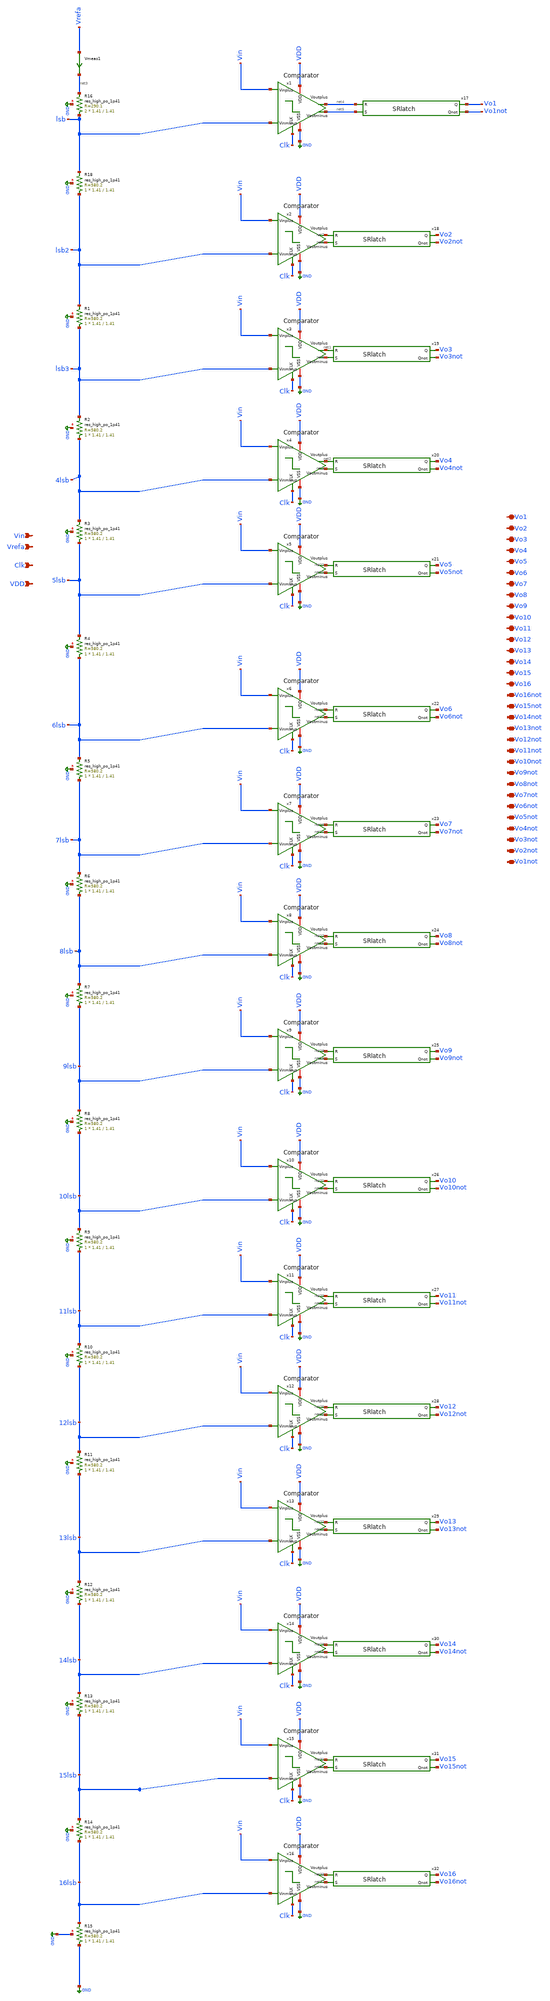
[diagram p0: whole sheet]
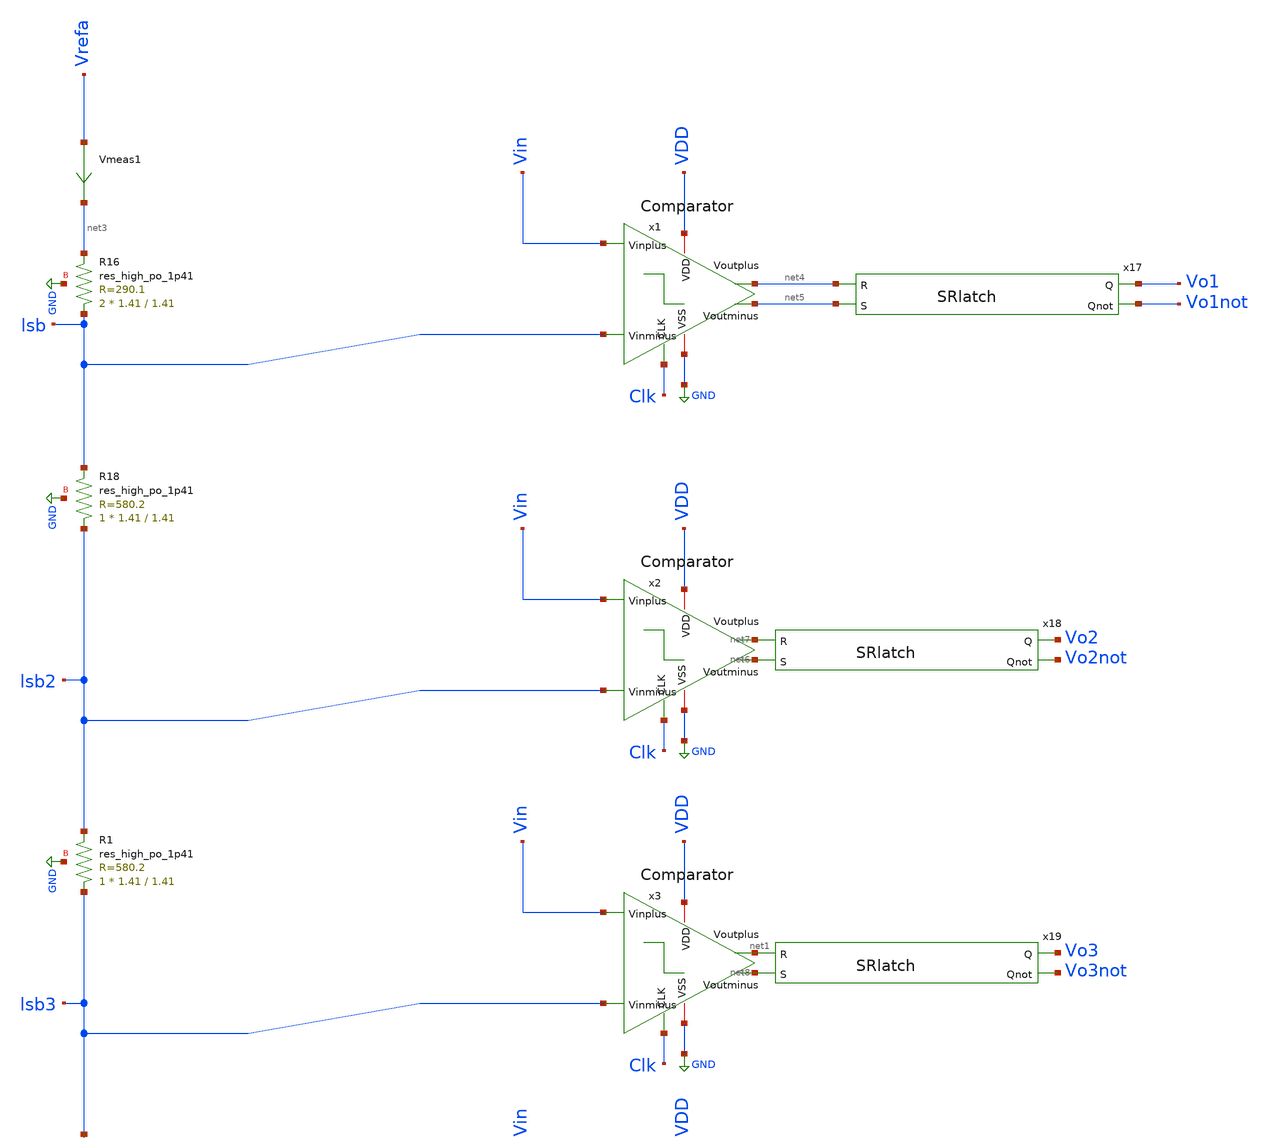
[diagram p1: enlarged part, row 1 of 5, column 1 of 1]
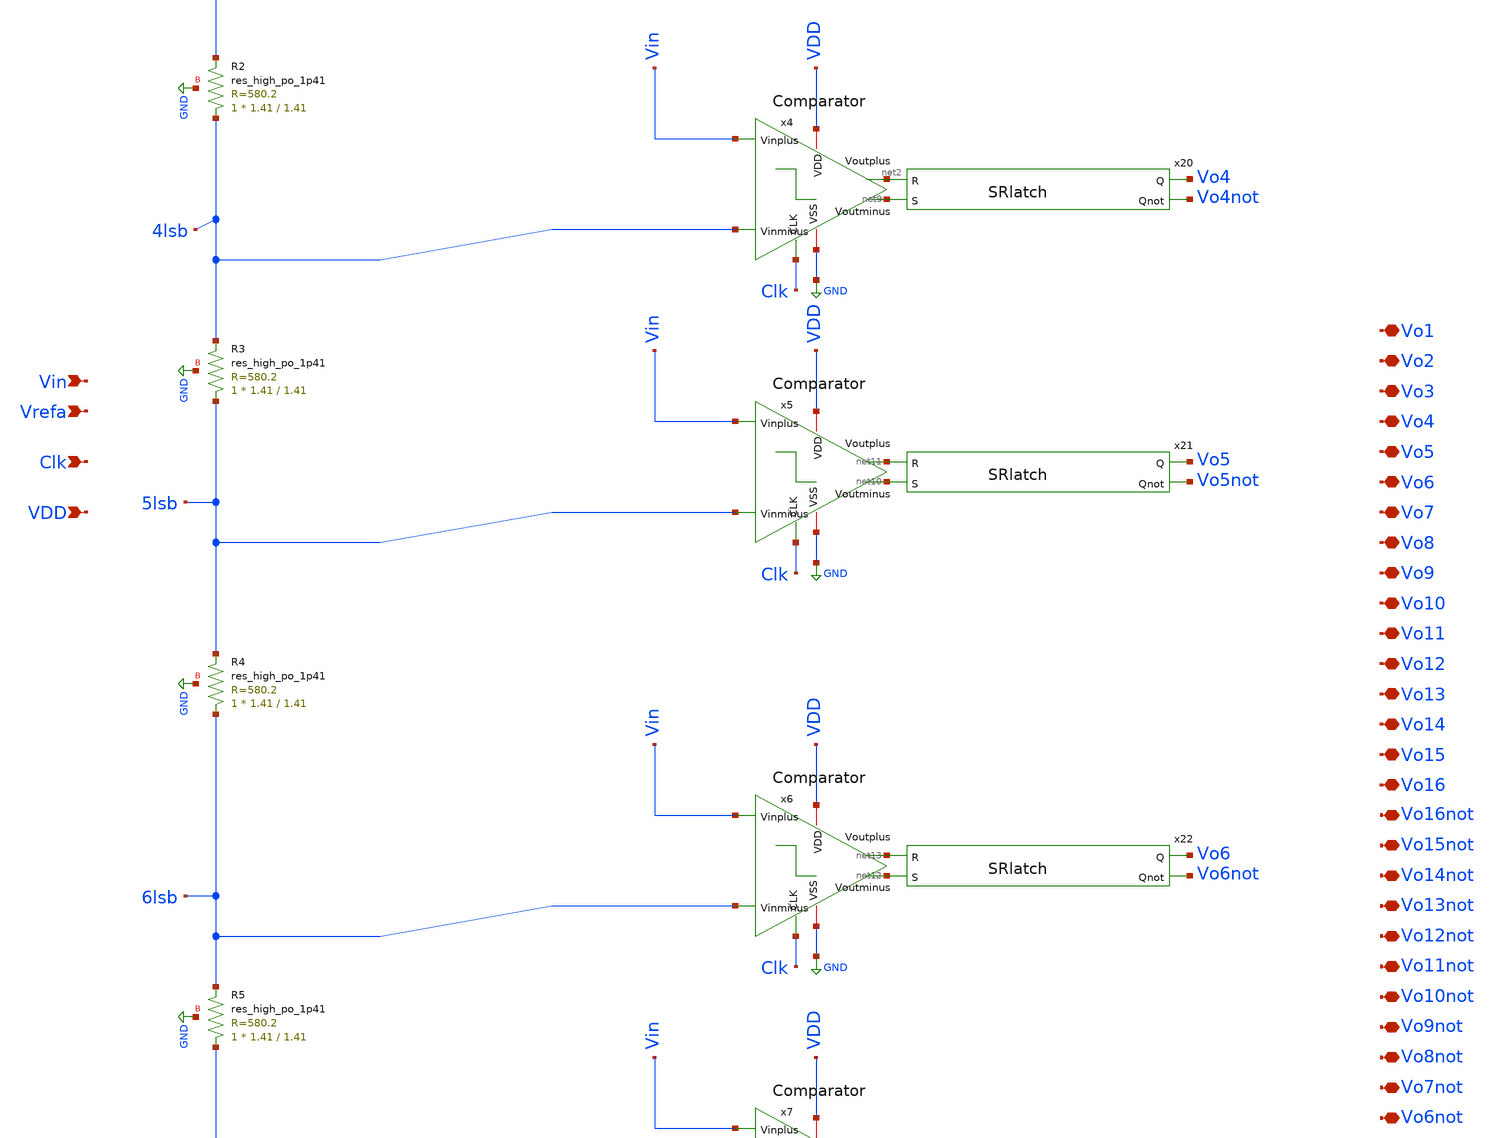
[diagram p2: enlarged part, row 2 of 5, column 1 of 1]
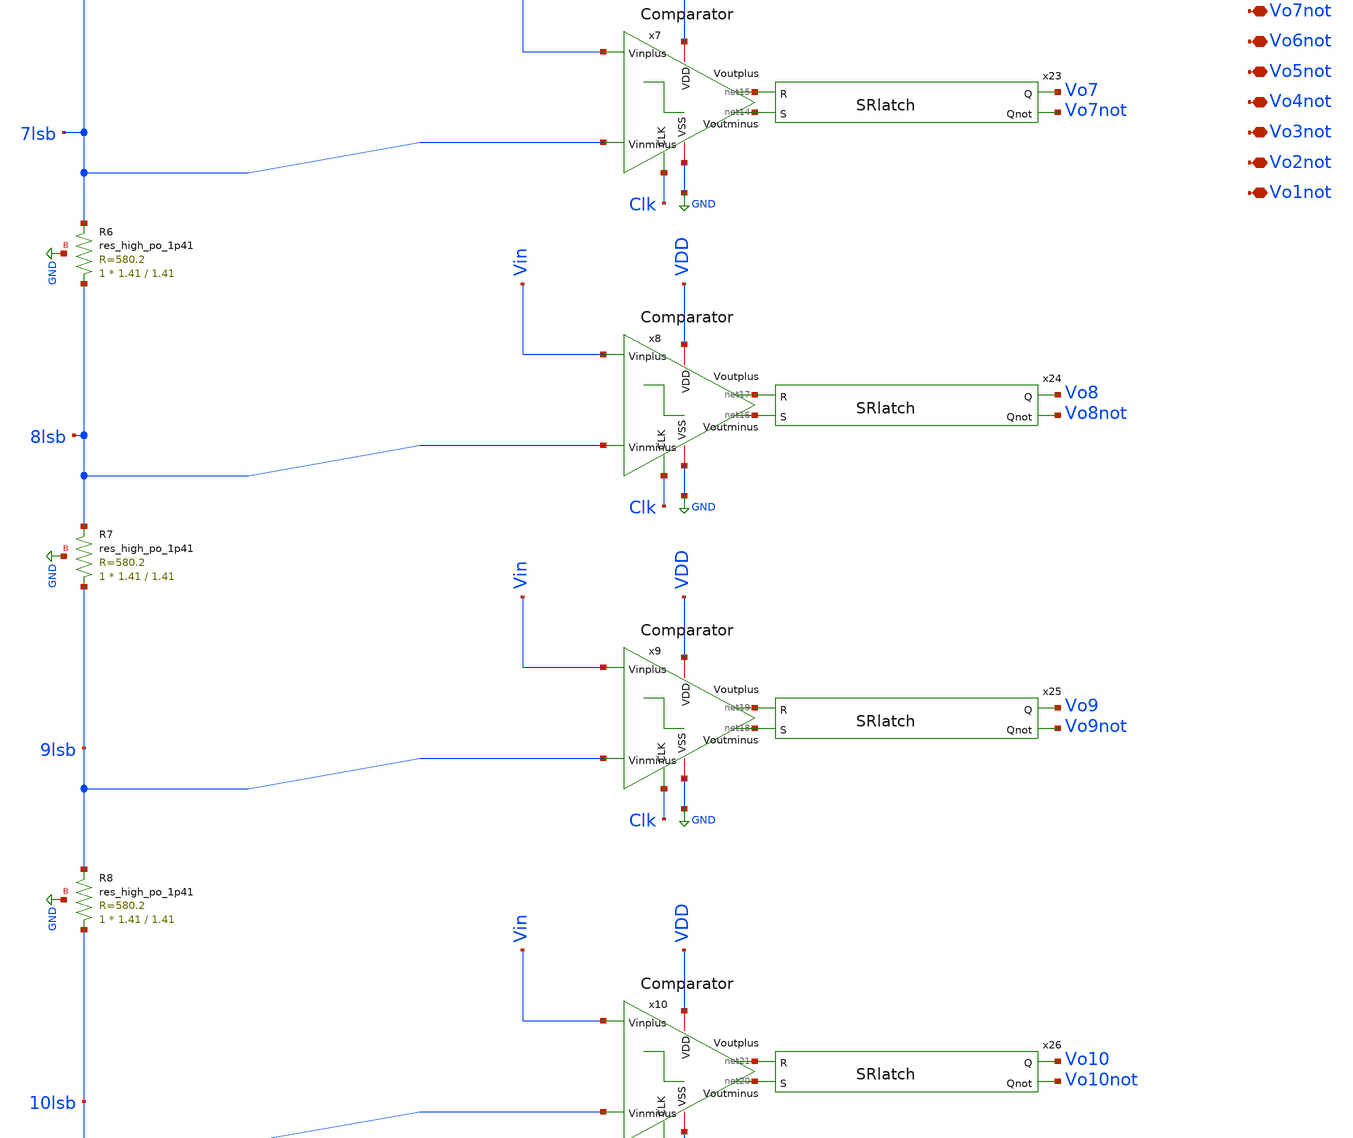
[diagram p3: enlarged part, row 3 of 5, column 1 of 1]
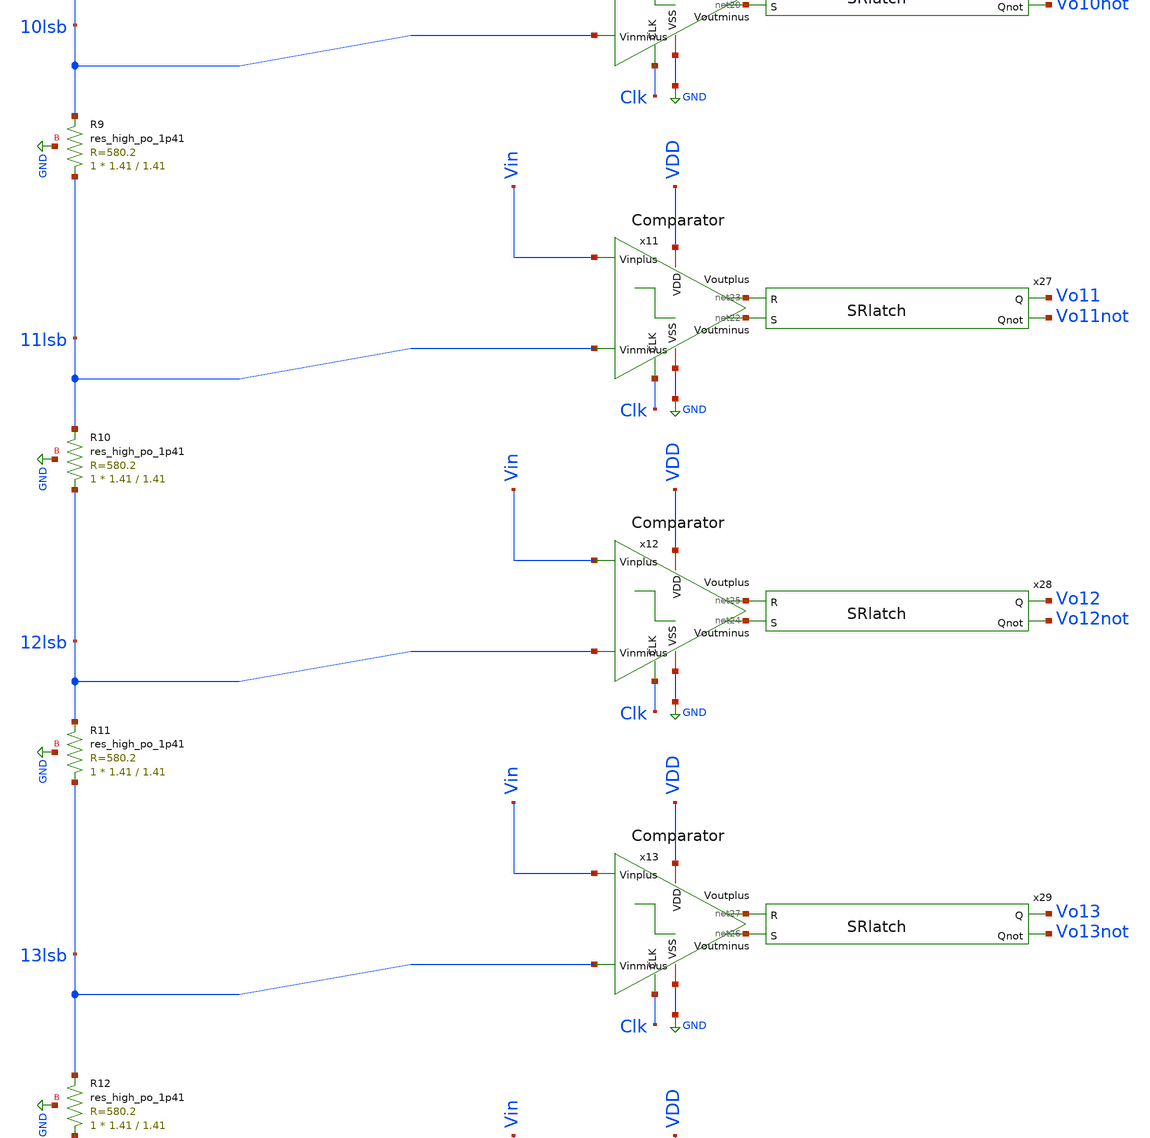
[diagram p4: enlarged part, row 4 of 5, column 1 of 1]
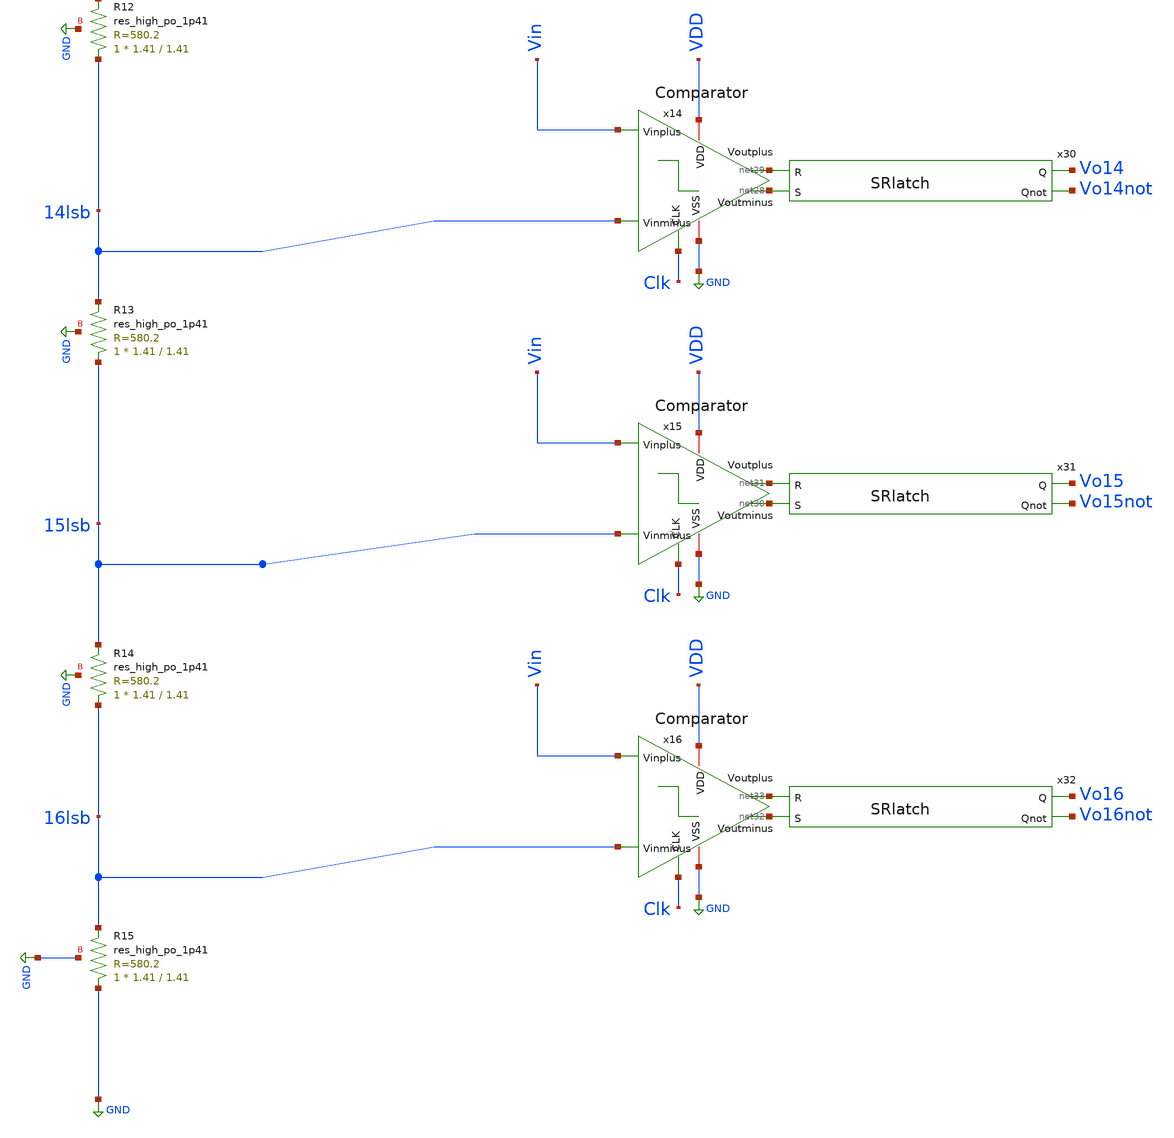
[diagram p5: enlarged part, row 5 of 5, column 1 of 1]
** sch_path: DataConverters/4bitADC.sch
**.subckt 4bitADC Vin Vrefa Clk VDD Vo1 Vo2 Vo3 Vo4 Vo5 Vo6 Vo7 Vo8 Vo9 Vo10 Vo11 Vo12 Vo13 Vo14
*+ Vo16 Vo16not Vo14not Vo13not Vo12not Vo11not Vo10not Vo9not Vo8not Vo7not Vo6not Vo5not Vo4not Vo3not
*+ Vo2not Vo1not Vo15 Vo15not
*.ipin Vin
*.ipin Vrefa
*.ipin Clk
*.ipin VDD
*.iopin Vo1
*.iopin Vo2
*.iopin Vo3
*.iopin Vo4
*.iopin Vo5
*.iopin Vo6
*.iopin Vo7
*.iopin Vo8
*.iopin Vo9
*.iopin Vo10
*.iopin Vo11
*.iopin Vo12
*.iopin Vo13
*.iopin Vo14
*.iopin Vo16
*.iopin Vo16not
*.iopin Vo14not
*.iopin Vo13not
*.iopin Vo12not
*.iopin Vo11not
*.iopin Vo10not
*.iopin Vo9not
*.iopin Vo8not
*.iopin Vo7not
*.iopin Vo6not
*.iopin Vo5not
*.iopin Vo4not
*.iopin Vo3not
*.iopin Vo2not
*.iopin Vo1not
*.iopin Vo15
*.iopin Vo15not
Vmeas1 Vrefa net3 0
.save i(vmeas1)
XR18 lsb2 lsb GND sky130_fd_pr__res_high_po_1p41 L=1.41 mult=1 m=1
XR1 lsb3 lsb2 GND sky130_fd_pr__res_high_po_1p41 L=1.41 mult=1 m=1
XR2 4lsb lsb3 GND sky130_fd_pr__res_high_po_1p41 L=1.41 mult=1 m=1
XR3 5lsb 4lsb GND sky130_fd_pr__res_high_po_1p41 L=1.41 mult=1 m=1
XR4 6lsb 5lsb GND sky130_fd_pr__res_high_po_1p41 L=1.41 mult=1 m=1
XR5 7lsb 6lsb GND sky130_fd_pr__res_high_po_1p41 L=1.41 mult=1 m=1
XR6 8lsb 7lsb GND sky130_fd_pr__res_high_po_1p41 L=1.41 mult=1 m=1
XR7 9lsb 8lsb GND sky130_fd_pr__res_high_po_1p41 L=1.41 mult=1 m=1
XR8 10lsb 9lsb GND sky130_fd_pr__res_high_po_1p41 L=1.41 mult=1 m=1
XR9 11lsb 10lsb GND sky130_fd_pr__res_high_po_1p41 L=1.41 mult=1 m=1
XR10 12lsb 11lsb GND sky130_fd_pr__res_high_po_1p41 L=1.41 mult=1 m=1
XR11 13lsb 12lsb GND sky130_fd_pr__res_high_po_1p41 L=1.41 mult=1 m=1
XR12 14lsb 13lsb GND sky130_fd_pr__res_high_po_1p41 L=1.41 mult=1 m=1
XR13 15lsb 14lsb GND sky130_fd_pr__res_high_po_1p41 L=1.41 mult=1 m=1
XR14 16lsb 15lsb GND sky130_fd_pr__res_high_po_1p41 L=1.41 mult=1 m=1
XR15 GND 16lsb GND sky130_fd_pr__res_high_po_1p41 L=1.41 mult=1 m=1
XR16 lsb net3 GND sky130_fd_pr__res_high_po_1p41 L=1.41 mult=2 m=2
x1 VDD net5 net4 Clk Vin lsb GND Comparator
x2 VDD net6 net7 Clk Vin lsb2 GND Comparator
x3 VDD net8 net1 Clk Vin lsb3 GND Comparator
x4 VDD net9 net2 Clk Vin 4lsb GND Comparator
x5 VDD net10 net11 Clk Vin 5lsb GND Comparator
x6 VDD net12 net13 Clk Vin 6lsb GND Comparator
x7 VDD net14 net15 Clk Vin 7lsb GND Comparator
x8 VDD net16 net17 Clk Vin 8lsb GND Comparator
x9 VDD net18 net19 Clk Vin 9lsb GND Comparator
x10 VDD net20 net21 Clk Vin 10lsb GND Comparator
x11 VDD net22 net23 Clk Vin 11lsb GND Comparator
x12 VDD net24 net25 Clk Vin 12lsb GND Comparator
x13 VDD net26 net27 Clk Vin 13lsb GND Comparator
x14 VDD net28 net29 Clk Vin 14lsb GND Comparator
x15 VDD net30 net31 Clk Vin 15lsb GND Comparator
x16 VDD net32 net33 Clk Vin 16lsb GND Comparator
x17 Vo1 Vo1not net4 net5 SRlatch
x18 Vo2 Vo2not net7 net6 SRlatch
x19 Vo3 Vo3not net1 net8 SRlatch
x20 Vo4 Vo4not net2 net9 SRlatch
x21 Vo5 Vo5not net11 net10 SRlatch
x22 Vo6 Vo6not net13 net12 SRlatch
x23 Vo7 Vo7not net15 net14 SRlatch
x24 Vo8 Vo8not net17 net16 SRlatch
x25 Vo9 Vo9not net19 net18 SRlatch
x26 Vo10 Vo10not net21 net20 SRlatch
x27 Vo11 Vo11not net23 net22 SRlatch
x28 Vo12 Vo12not net25 net24 SRlatch
x29 Vo13 Vo13not net27 net26 SRlatch
x30 Vo14 Vo14not net29 net28 SRlatch
x31 Vo15 Vo15not net31 net30 SRlatch
x32 Vo16 Vo16not net33 net32 SRlatch
**.ends
.GLOBAL GND
.end
